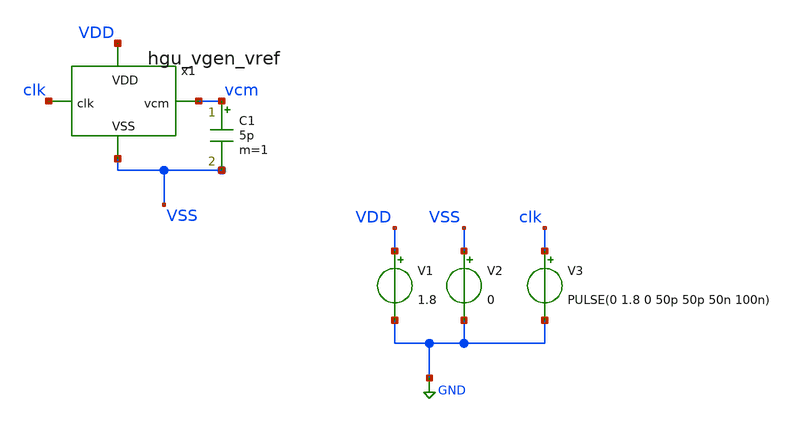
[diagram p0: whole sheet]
** sch_path: hgu/tb/tb_hgu_vgen_vref.sch
**.subckt tb_hgu_vgen_vref
x1 VDD VSS clk vcm hgu_vgen_vref
V1 VDD GND 1.8
V2 VSS GND 0
V3 clk GND PULSE(0 1.8 0 50p 50p 50n 100n)
C1 vcm VSS 5p m=1
**** begin user architecture code



.lib /foss/pdks/sky130A/libs.tech/ngspice/sky130.lib.spice tt
.include /foss/pdks/sky130A/libs.ref/sky130_fd_sc_hd/spice/sky130_fd_sc_hd.spice


.tran 1ns 5000ns
.control
    run
    plot V(clk)+2 V(vcm)
.endc
.save all



**** end user architecture code
**.ends
.GLOBAL GND
.end
